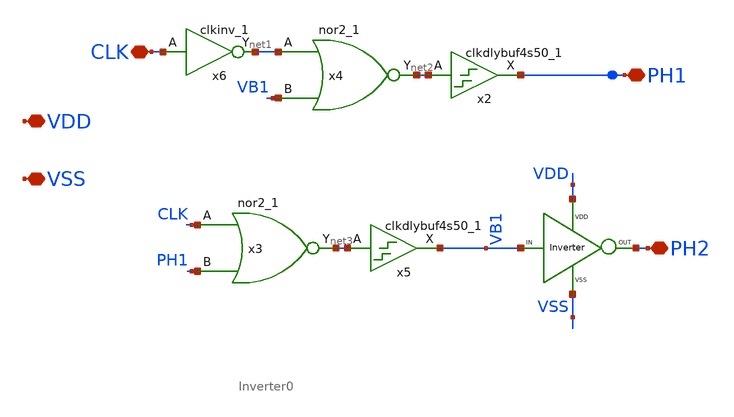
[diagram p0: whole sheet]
** sch_path: xschem/DC_DC_Converter_xschem/OTHERS/DC_DC_Converter_JV11/Non_Overlap_Clk/Non_over_clk_2.sch
**.subckt Non_over_clk_2 VDD VSS CLK PH1 PH2
*.iopin VDD
*.iopin VSS
*.iopin CLK
*.iopin PH1
*.iopin PH2
x3 CLK PH1 VSS VSS VDD VDD net3 sky130_fd_sc_hd__nor2_1
x4 net1 VB1 VSS VSS VDD VDD net2 sky130_fd_sc_hd__nor2_1
x6 CLK VSS VSS VDD VDD net1 sky130_fd_sc_hd__clkinv_1
x2 net2 VSS VSS VDD VDD PH1 sky130_fd_sc_hd__clkdlybuf4s50_1
x5 net3 VSS VSS VDD VDD VB1 sky130_fd_sc_hd__clkdlybuf4s50_1
X1 VB1 PH2 VDD VSS Inverter0
**.ends

* expanding   symbol:  DC_DC_Converter/Inverter_0/Inverter0.sym # of pins=4
** sym_path: xschem/DC_DC_Converter_xschem/DC_DC_Converter/Delay_block_revised/Inverter_0/Inverter0.sym
** sch_path: xschem/DC_DC_Converter_xschem/DC_DC_Converter/Delay_block_revised/Inverter_0/Inverter0.sch
.subckt Inverter0 VIN VOUT VDD VSS
*.ipin VIN
*.iopin VDD
*.iopin VSS
*.opin VOUT
XM1 VOUT VIN VSS VSS sky130_fd_pr__nfet_01v8 L=0.15 W=0.4 nf=1 ad='int((nf+1)/2) * W/nf * 0.29' as='int((nf+2)/2) * W/nf * 0.29'
+ pd='2*int((nf+1)/2) * (W/nf + 0.29)' ps='2*int((nf+2)/2) * (W/nf + 0.29)' nrd='0.29 / W' nrs='0.29 / W'
+ sa=0 sb=0 sd=0 mult=1 m=1
XM2 VOUT VIN VDD VDD sky130_fd_pr__pfet_01v8 L=0.15 W=1.2 nf=1 ad='int((nf+1)/2) * W/nf * 0.29' as='int((nf+2)/2) * W/nf * 0.29'
+ pd='2*int((nf+1)/2) * (W/nf + 0.29)' ps='2*int((nf+2)/2) * (W/nf + 0.29)' nrd='0.29 / W' nrs='0.29 / W'
+ sa=0 sb=0 sd=0 mult=1 m=1
.ends

.end
